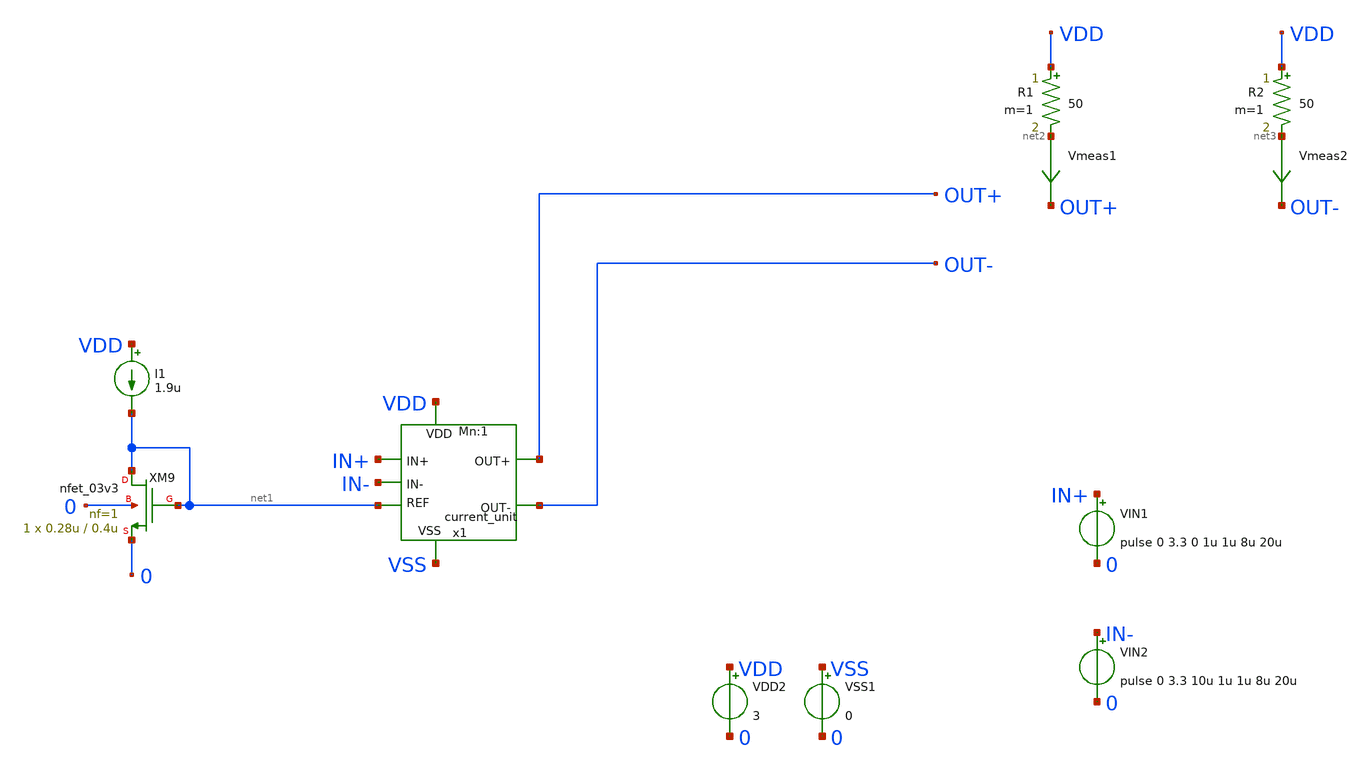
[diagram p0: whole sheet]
** sch_path: DAC/xschem/analog_cell/test/test)CCU.sch
**.subckt test)CCU
R1 VDD net2 50 m=1
R2 VDD net3 50 m=1
Vmeas1 net2 OUT+ 0
.save i(vmeas1)
Vmeas2 net3 OUT- 0
.save i(vmeas2)
VIN1 IN+ 0 pulse 0 3.3 0 1u 1u 8u 20u
VIN2 IN- 0 pulse 0 3.3 10u 1u 1u 8u 20u
VDD2 VDD 0 3
VSS1 VSS 0 0
x1 VDD VSS net1 IN+ IN- OUT+ OUT- current_unit Mn=1 Wp=0.3u Wn=0.3u
I1 VDD net1 1.9u
XM9 net1 net1 0 0 nfet_03v3 L=0.4u W=0.28u nf=1 ad='int((nf+1)/2) * W/nf * 0.18u' as='int((nf+2)/2) * W/nf * 0.18u'
+ pd='2*int((nf+1)/2) * (W/nf + 0.18u)' ps='2*int((nf+2)/2) * (W/nf + 0.18u)' nrd='0.18u / W' nrs='0.18u / W'
+ sa=0 sb=0 sd=0 m=1
**** begin user architecture code

.include $::180MCU_MODELS/design.ngspice
.lib $::180MCU_MODELS/sm141064.ngspice typical
.lib $::180MCU_MODELS/sm141064.ngspice res_typical
.lib $::180MCU_MODELS/sm141064.ngspice moscap_typical
* .lib $::180MCU_MODELS/sm141064.ngspice res_statistical




.options savecurrents

.control
	*dc I0 1u 4u 0.1u
	tran 0.1u 100u

	*plot v(d3)
 	*plot v(b2)-v(s3)-@m.xm3.m0[vth] v(b1)-@m.xm4.m0[vth]
	*plot @m.xm3.m0[vth] @m.xm4.m0[vth]
	plot V(IN+) V(IN-)
	plot i(Vmeas1) i(Vmeas2)

.endc

.save all


**** end user architecture code
**.ends

* expanding   symbol:  designs/analog_cell/current_unit.sym # of pins=7
** sym_path: DAC/xschem/analog_cell/current_unit.sym
** sch_path: DAC/xschem/analog_cell/current_unit.sch
.subckt current_unit VDD VSS REF IN+ IN- OUT+ OUT-  Mn=1 Wp=0.3u Wn=0.3u
*.ipin REF
*.ipin IN+
*.ipin IN-
*.opin OUT+
*.opin OUT-
*.ipin VSS
*.ipin VDD
XM3 net1 net2 net4 VSS nfet_03v3 L=0.4u W=Wn nf=1 ad='int((nf+1)/2) * W/nf * 0.18u' as='int((nf+2)/2) * W/nf * 0.18u'
+ pd='2*int((nf+1)/2) * (W/nf + 0.18u)' ps='2*int((nf+2)/2) * (W/nf + 0.18u)' nrd='0.18u / W' nrs='0.18u / W'
+ sa=0 sb=0 sd=0 m=Mn
XM4 net4 net3 VSS VSS nfet_03v3 L=0.4u W=Wn nf=1 ad='int((nf+1)/2) * W/nf * 0.18u' as='int((nf+2)/2) * W/nf * 0.18u'
+ pd='2*int((nf+1)/2) * (W/nf + 0.18u)' ps='2*int((nf+2)/2) * (W/nf + 0.18u)' nrd='0.18u / W' nrs='0.18u / W'
+ sa=0 sb=0 sd=0 m=Mn
XM5 net2 net2 net3 VSS nfet_03v3 L=0.4u W=Wn nf=1 ad='int((nf+1)/2) * W/nf * 0.18u' as='int((nf+2)/2) * W/nf * 0.18u'
+ pd='2*int((nf+1)/2) * (W/nf + 0.18u)' ps='2*int((nf+2)/2) * (W/nf + 0.18u)' nrd='0.18u / W' nrs='0.18u / W'
+ sa=0 sb=0 sd=0 m=1
XM6 net3 net3 VSS VSS nfet_03v3 L=0.4u W=Wn nf=1 ad='int((nf+1)/2) * W/nf * 0.18u' as='int((nf+2)/2) * W/nf * 0.18u'
+ pd='2*int((nf+1)/2) * (W/nf + 0.18u)' ps='2*int((nf+2)/2) * (W/nf + 0.18u)' nrd='0.18u / W' nrs='0.18u / W'
+ sa=0 sb=0 sd=0 m=1
XM1 net5 net5 VDD VDD pfet_03v3 L=0.28u W=0.4u nf=1 ad='int((nf+1)/2) * W/nf * 0.18u' as='int((nf+2)/2) * W/nf * 0.18u'
+ pd='2*int((nf+1)/2) * (W/nf + 0.18u)' ps='2*int((nf+2)/2) * (W/nf + 0.18u)' nrd='0.18u / W' nrs='0.18u / W'
+ sa=0 sb=0 sd=0 m=1
XM2 net2 net5 VDD VDD pfet_03v3 L=0.28u W=Wp nf=1 ad='int((nf+1)/2) * W/nf * 0.18u' as='int((nf+2)/2) * W/nf * 0.18u'
+ pd='2*int((nf+1)/2) * (W/nf + 0.18u)' ps='2*int((nf+2)/2) * (W/nf + 0.18u)' nrd='0.18u / W' nrs='0.18u / W'
+ sa=0 sb=0 sd=0 m=1
XM7 OUT+ IN+ net1 VDD nfet_03v3 L=0.3u W=Wn nf=1 ad='int((nf+1)/2) * W/nf * 0.18u' as='int((nf+2)/2) * W/nf * 0.18u'
+ pd='2*int((nf+1)/2) * (W/nf + 0.18u)' ps='2*int((nf+2)/2) * (W/nf + 0.18u)' nrd='0.18u / W' nrs='0.18u / W'
+ sa=0 sb=0 sd=0 m=1
XM8 OUT- IN- net1 VDD nfet_03v3 L=0.3u W=Wn nf=1 ad='int((nf+1)/2) * W/nf * 0.18u' as='int((nf+2)/2) * W/nf * 0.18u'
+ pd='2*int((nf+1)/2) * (W/nf + 0.18u)' ps='2*int((nf+2)/2) * (W/nf + 0.18u)' nrd='0.18u / W' nrs='0.18u / W'
+ sa=0 sb=0 sd=0 m=1
XM9 net5 REF VSS VSS nfet_03v3 L=0.4u W=0.28u nf=1 ad='int((nf+1)/2) * W/nf * 0.18u' as='int((nf+2)/2) * W/nf * 0.18u'
+ pd='2*int((nf+1)/2) * (W/nf + 0.18u)' ps='2*int((nf+2)/2) * (W/nf + 0.18u)' nrd='0.18u / W' nrs='0.18u / W'
+ sa=0 sb=0 sd=0 m=Mn
.ends

.end
